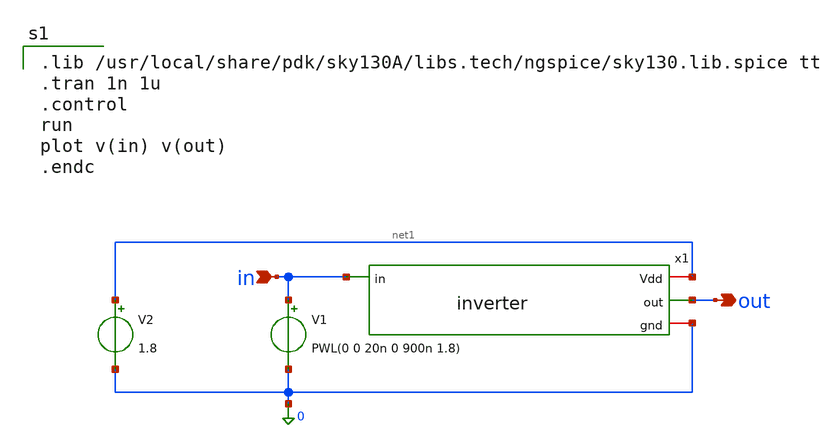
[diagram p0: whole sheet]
** sch_path: analog/tim-edwards-ws/inverter/xschem/inverter_tb.sch
**.subckt inverter_tb out in
*.opin out
*.ipin in
x1 net1 in out 0 inverter
V1 in 0 PWL(0 0 20n 0 900n 1.8)
V2 net1 0 1.8
**** begin user architecture code

.lib /usr/local/share/pdk/sky130A/libs.tech/ngspice/sky130.lib.spice tt
.tran 1n 1u
.control
run
plot v(in) v(out)
.endc

**** end user architecture code
**.ends

* expanding   symbol:  inverter.sym # of pins=4
** sym_path: analog/tim-edwards-ws/inverter/xschem/inverter.sym
** sch_path: analog/tim-edwards-ws/inverter/xschem/inverter.sch
.subckt inverter Vdd in out gnd
*.ipin in
*.opin out
*.iopin gnd
*.iopin Vdd
XM1 out in gnd gnd sky130_fd_pr__nfet_01v8 L=0.18 W=4.5 nf=3 ad='int((3 + 1)/2) * 4.5 / 3 * 0.29' as='int((3 + 2)/2) * 4.5 / 3 * 0.29'
+ pd='2*int((3 + 1)/2) * (4.5 / 3 + 0.29)' ps='2*int((3 + 2)/2) * (4.5 / 3 + 0.29)' nrd='0.29 / 4.5 ' nrs='0.29 / 4.5 '
+ sa=0 sb=0 sd=0 mult=1 m=1
XM2 out in Vdd VDD sky130_fd_pr__pfet_01v8 L=0.18 W=3 nf=3 ad='int((3 + 1)/2) * 3 / 3 * 0.29' as='int((3 + 2)/2) * 3 / 3 * 0.29'
+ pd='2*int((3 + 1)/2) * (3 / 3 + 0.29)' ps='2*int((3 + 2)/2) * (3 / 3 + 0.29)' nrd='0.29 / 3 ' nrs='0.29 / 3 '
+ sa=0 sb=0 sd=0 mult=1 m=1
.ends

.end
